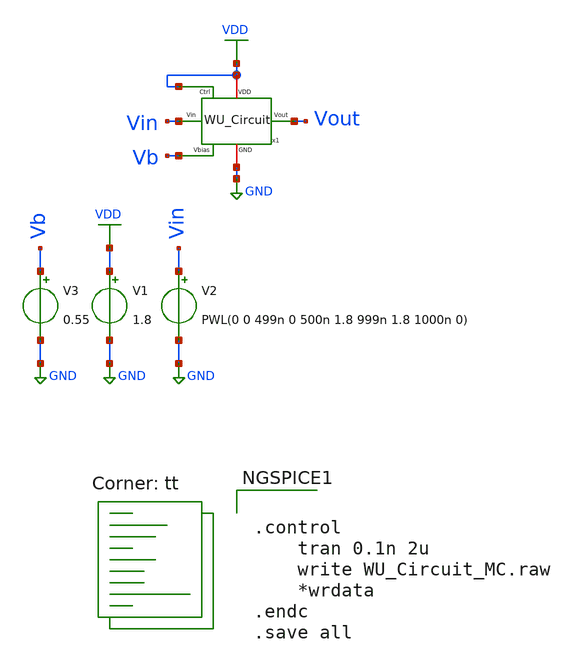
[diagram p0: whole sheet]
** sch_path: SNN/WU_Circuit_tb.sch
**.subckt WU_Circuit_tb
V1 VDD GND 1.8
V2 Vin GND PWL(0 0 499n 0 500n 1.8 999n 1.8 1000n 0)
V3 Vb GND 0.55
x1 Vb VDD Vin GND VDD Vout WU_Circuit
**** begin user architecture code
.lib $::SKYWATER_MODELS/sky130.lib.spice tt


.control
	tran 0.1n 2u
	write WU_Circuit_MC.raw
	*wrdata
.endc
.save all


**** end user architecture code
**.ends
.GLOBAL GND
.GLOBAL VDD
.end
